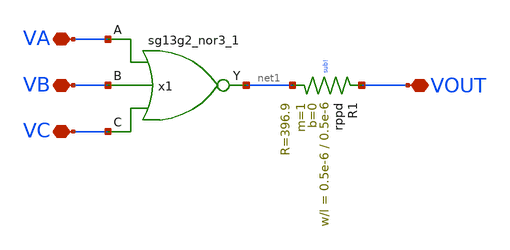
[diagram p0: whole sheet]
** sch_path: example/nor3_res.sch
**.subckt nor3_res VOUT VA VB VC
*.iopin VOUT
*.iopin VA
*.iopin VB
*.iopin VC
x1 net1 VA VB VC VDD VSS sg13g2_nor3_1
XR1 VOUT net1 sub! rppd w=0.5e-6 l=0.5e-6 m=1 b=0 mm_ok=1
**.ends

* expanding   symbol:  sg13g2_stdcells/sg13g2_nor3_1.sym # of pins=4
** sym_path: sg13g2_stdcells/sg13g2_nor3_1.sym
** sch_path: sg13g2_stdcells/sg13g2_nor3_1.sch
.subckt sg13g2_nor3_1 Y A B C VDD VSS
*.ipin B
*.iopin VDD
*.iopin VSS
*.opin Y
*.ipin A
*.ipin C
XM1 Y A VSS VSS sg13_lv_nmos w=770.00n l=130.00n ng=1 m=1 mm_ok=1
XM2 Y B VSS VSS sg13_lv_nmos w=770.00n l=130.00n ng=1 m=1 mm_ok=1
XM3 Y C VSS VSS sg13_lv_nmos w=770.00n l=130.00n ng=1 m=1 mm_ok=1
XM4 net1 A VDD VDD sg13_lv_pmos w=1.12u l=130.00n ng=1 m=1 mm_ok=1
XM5 net2 B net1 VDD sg13_lv_pmos w=1.12u l=130.00n ng=1 m=1 mm_ok=1
XM6 Y C net2 VDD sg13_lv_pmos w=1.12u l=130.00n ng=1 m=1 mm_ok=1
.ends

.end
